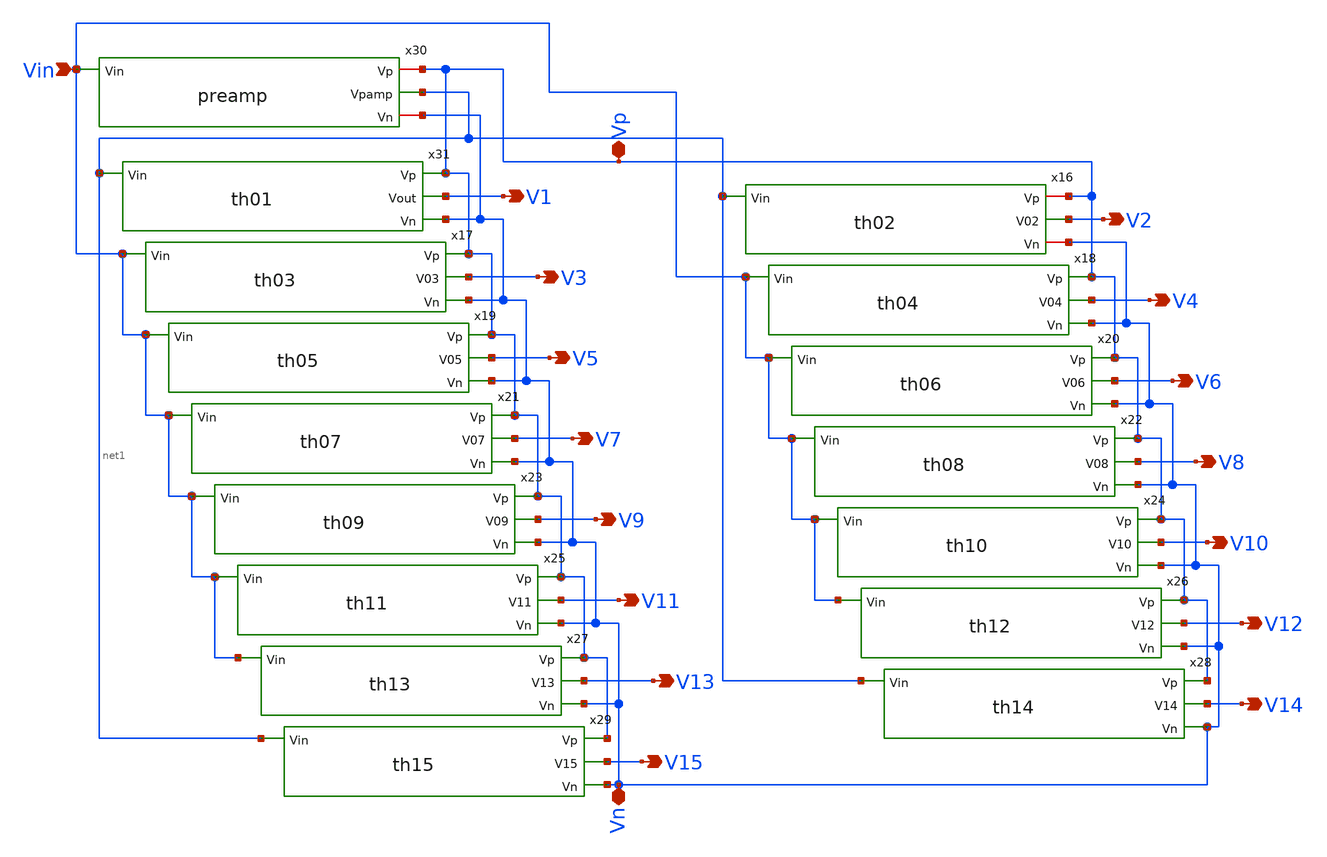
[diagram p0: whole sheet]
** sch_path: xschem/Vth_sch/Symbol/Analog.sch
**.subckt Analog V1 Vin V2 V3 V4 V5 V6 V7 V8 V9 V10 V11 V12 V13 V14 V15 Vp Vn
*.opin V1
*.ipin Vin
*.opin V2
*.opin V3
*.opin V4
*.opin V5
*.opin V6
*.opin V7
*.opin V8
*.opin V9
*.opin V10
*.opin V11
*.opin V12
*.opin V13
*.opin V14
*.opin V15
*.iopin Vp
*.iopin Vn
x16 Vp net1 V2 Vn th02
x17 Vp V3 Vin Vn th03
x18 Vp V4 Vin Vn th04
x19 Vp V5 Vin Vn th05
x20 Vp Vin V6 Vn th06
x21 Vp Vin V7 Vn th07
x22 Vp V8 Vin Vn th08
x23 Vp V9 Vin Vn th09
x24 Vp V10 Vin Vn th10
x25 Vp V11 Vin Vn th11
x26 Vp V12 Vin Vn th12
x27 Vp V13 Vin Vn th13
x28 Vp V14 net1 Vn th14
x29 Vp V15 net1 Vn th15
x30 Vp Vin net1 Vn preamp
x31 Vp net1 V1 Vn th01
**.ends
.end
